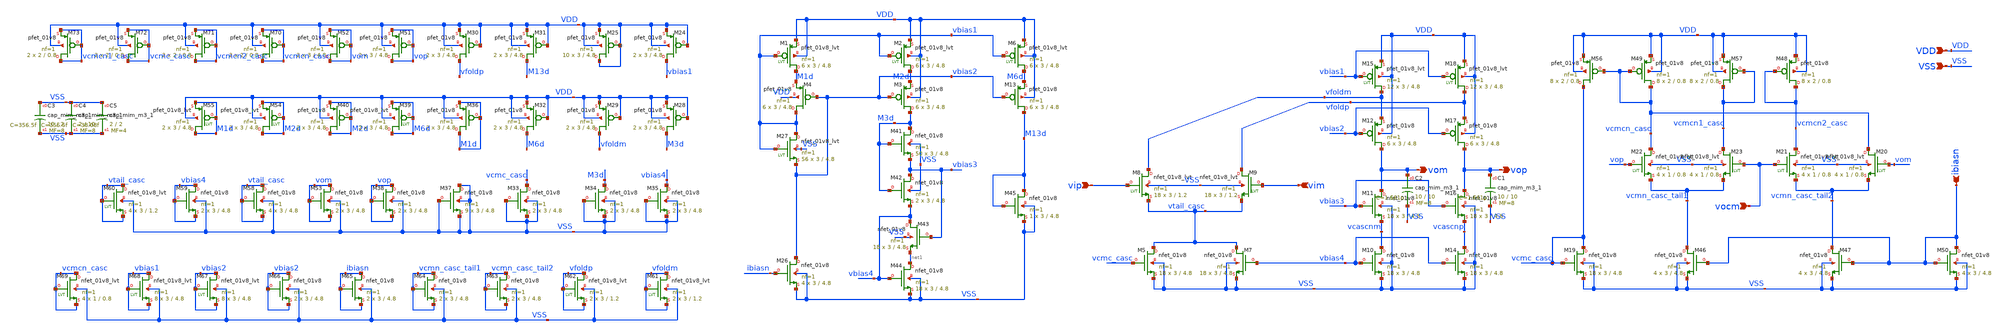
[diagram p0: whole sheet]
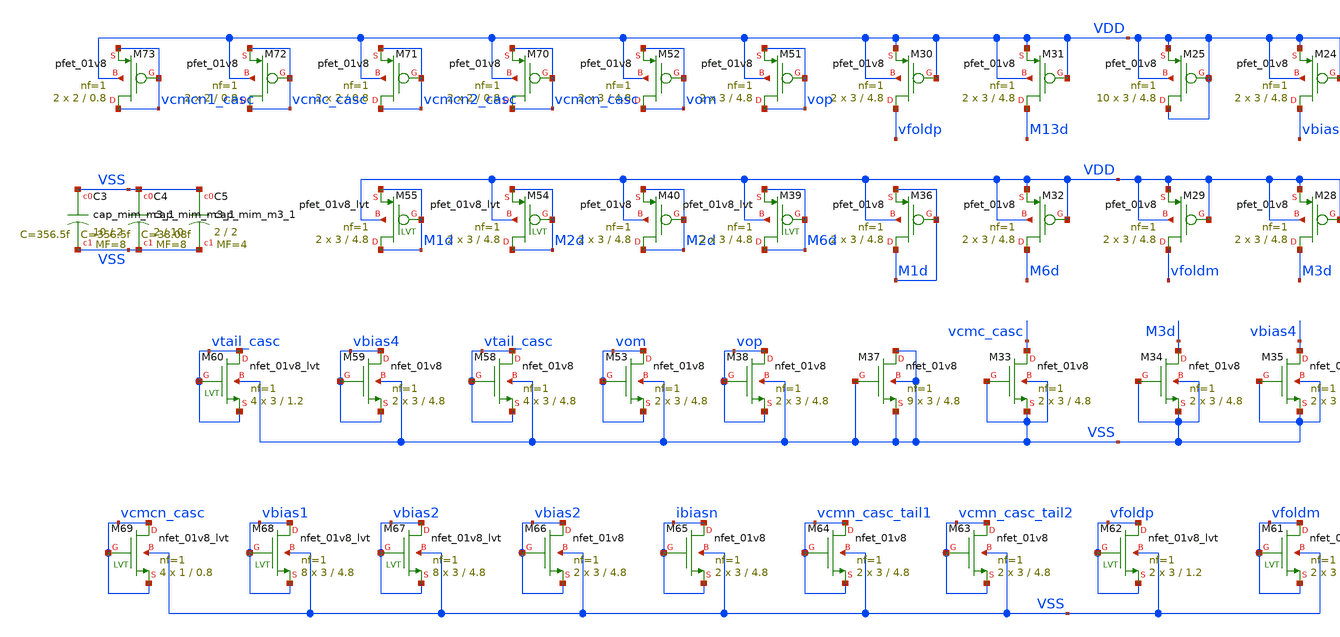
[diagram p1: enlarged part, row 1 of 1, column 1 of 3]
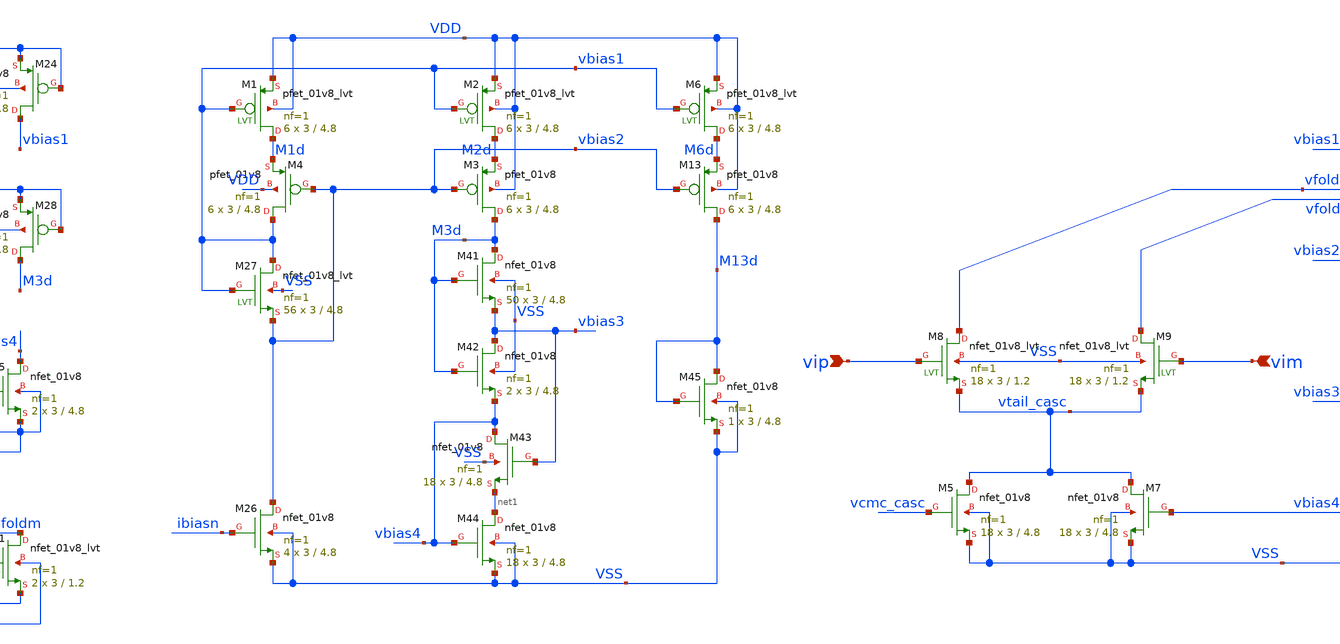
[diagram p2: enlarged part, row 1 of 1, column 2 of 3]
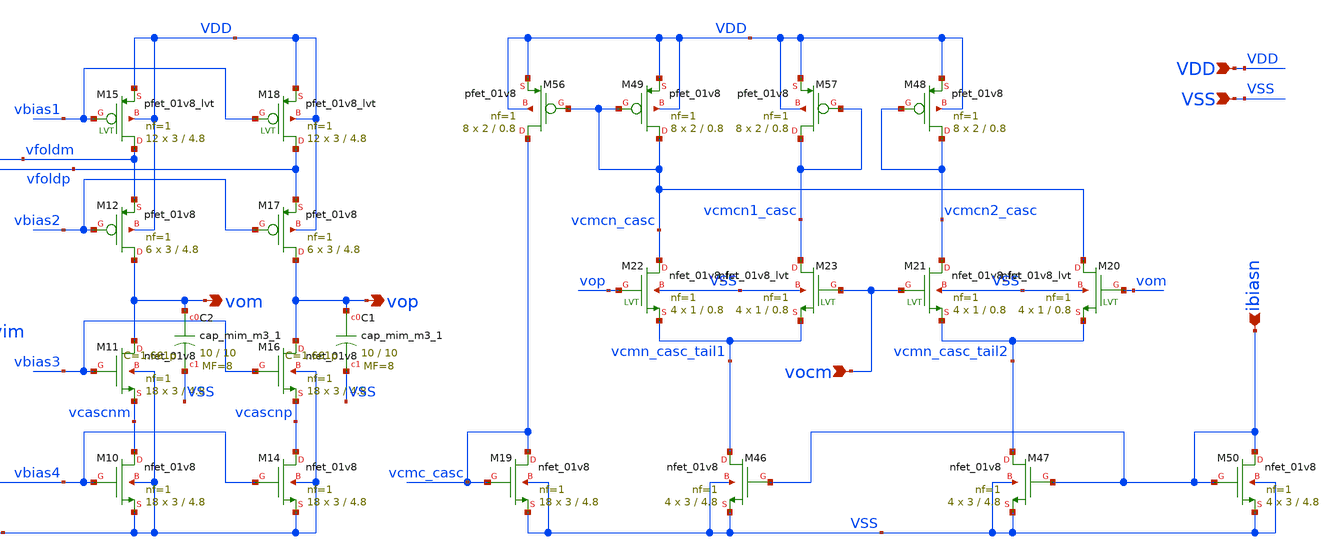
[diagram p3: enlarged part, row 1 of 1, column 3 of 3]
** sch_path: designs/diff_fold_casc_ota_lvs.sch
* Copyright 2020 Stefan Frederik Schippers
* Licensed under the Apache License, Version 2.0 (the "License");
* you may not use this file except in compliance with the License.
* You may obtain a copy of the License at
* https://www.apache.org/licenses/LICENSE-2.0
* Unless required by applicable law or agreed to in writing, software
* distributed under the License is distributed on an "AS IS" BASIS,
* WITHOUT WARRANTIES OR CONDITIONS OF ANY KIND, either express or implied.
* See the License for the specific language governing permissions and
* limitations under the License.
**.subckt diff_fold_casc_ota_lvs vop vom vip vim vocm ibiasn VDD VSS
*.opin vop
*.opin vom
*.ipin vip
*.ipin vim
*.ipin vocm
*.ipin ibiasn
*.ipin VDD
*.ipin VSS
XM41 M3d M3d vbias3 VSS sky130_fd_pr__nfet_01v8 L=4.8 W=3 nf=1 ad='int((nf+1)/2) * W/nf * 0.29' as='int((nf+2)/2) * W/nf * 0.29'
+ pd='2*int((nf+1)/2) * (W/nf + 0.29)' ps='2*int((nf+2)/2) * (W/nf + 0.29)' nrd='0.29 / W' nrs='0.29 / W'
+ sa=0 sb=0 sd=0 mult=50 m=50
XM42 vbias3 M3d vbias4 VSS sky130_fd_pr__nfet_01v8 L=4.8 W=3 nf=1 ad='int((nf+1)/2) * W/nf * 0.29' as='int((nf+2)/2) * W/nf * 0.29'
+ pd='2*int((nf+1)/2) * (W/nf + 0.29)' ps='2*int((nf+2)/2) * (W/nf + 0.29)' nrd='0.29 / W' nrs='0.29 / W'
+ sa=0 sb=0 sd=0 mult=2 m=2
XM43 vbias4 vbias3 net1 VSS sky130_fd_pr__nfet_01v8 L=4.8 W=3 nf=1 ad='int((nf+1)/2) * W/nf * 0.29' as='int((nf+2)/2) * W/nf * 0.29'
+ pd='2*int((nf+1)/2) * (W/nf + 0.29)' ps='2*int((nf+2)/2) * (W/nf + 0.29)' nrd='0.29 / W' nrs='0.29 / W'
+ sa=0 sb=0 sd=0 mult=18 m=18
XM44 net1 vbias4 VSS VSS sky130_fd_pr__nfet_01v8 L=4.8 W=3 nf=1 ad='int((nf+1)/2) * W/nf * 0.29' as='int((nf+2)/2) * W/nf * 0.29'
+ pd='2*int((nf+1)/2) * (W/nf + 0.29)' ps='2*int((nf+2)/2) * (W/nf + 0.29)' nrd='0.29 / W' nrs='0.29 / W'
+ sa=0 sb=0 sd=0 mult=18 m=18
XM45 M13d M13d VSS VSS sky130_fd_pr__nfet_01v8 L=4.8 W=3 nf=1 ad='int((nf+1)/2) * W/nf * 0.29' as='int((nf+2)/2) * W/nf * 0.29'
+ pd='2*int((nf+1)/2) * (W/nf + 0.29)' ps='2*int((nf+2)/2) * (W/nf + 0.29)' nrd='0.29 / W' nrs='0.29 / W'
+ sa=0 sb=0 sd=0 mult=1 m=1
XM46 vcmn_casc_tail1 ibiasn VSS VSS sky130_fd_pr__nfet_01v8 L=4.8 W=3 nf=1 ad='int((nf+1)/2) * W/nf * 0.29'
+ as='int((nf+2)/2) * W/nf * 0.29' pd='2*int((nf+1)/2) * (W/nf + 0.29)' ps='2*int((nf+2)/2) * (W/nf + 0.29)'
+ nrd='0.29 / W' nrs='0.29 / W' sa=0 sb=0 sd=0 mult=4 m=4
XM47 vcmn_casc_tail2 ibiasn VSS VSS sky130_fd_pr__nfet_01v8 L=4.8 W=3 nf=1 ad='int((nf+1)/2) * W/nf * 0.29'
+ as='int((nf+2)/2) * W/nf * 0.29' pd='2*int((nf+1)/2) * (W/nf + 0.29)' ps='2*int((nf+2)/2) * (W/nf + 0.29)'
+ nrd='0.29 / W' nrs='0.29 / W' sa=0 sb=0 sd=0 mult=4 m=4
XM48 vcmcn2_casc vcmcn2_casc VDD VDD sky130_fd_pr__pfet_01v8 L=0.8 W=2 nf=1 ad='int((nf+1)/2) * W/nf * 0.29'
+ as='int((nf+2)/2) * W/nf * 0.29' pd='2*int((nf+1)/2) * (W/nf + 0.29)' ps='2*int((nf+2)/2) * (W/nf + 0.29)'
+ nrd='0.29 / W' nrs='0.29 / W' sa=0 sb=0 sd=0 mult=8 m=8
XM49 vcmcn_casc vcmcn_casc VDD VDD sky130_fd_pr__pfet_01v8 L=0.8 W=2 nf=1 ad='int((nf+1)/2) * W/nf * 0.29'
+ as='int((nf+2)/2) * W/nf * 0.29' pd='2*int((nf+1)/2) * (W/nf + 0.29)' ps='2*int((nf+2)/2) * (W/nf + 0.29)'
+ nrd='0.29 / W' nrs='0.29 / W' sa=0 sb=0 sd=0 mult=8 m=8
XM50 ibiasn ibiasn VSS VSS sky130_fd_pr__nfet_01v8 L=4.8 W=3 nf=1 ad='int((nf+1)/2) * W/nf * 0.29' as='int((nf+2)/2) * W/nf * 0.29'
+ pd='2*int((nf+1)/2) * (W/nf + 0.29)' ps='2*int((nf+2)/2) * (W/nf + 0.29)' nrd='0.29 / W' nrs='0.29 / W'
+ sa=0 sb=0 sd=0 mult=4 m=4
XM56 vcmc_casc vcmcn_casc VDD VDD sky130_fd_pr__pfet_01v8 L=0.8 W=2 nf=1 ad='int((nf+1)/2) * W/nf * 0.29'
+ as='int((nf+2)/2) * W/nf * 0.29' pd='2*int((nf+1)/2) * (W/nf + 0.29)' ps='2*int((nf+2)/2) * (W/nf + 0.29)'
+ nrd='0.29 / W' nrs='0.29 / W' sa=0 sb=0 sd=0 mult=8 m=8
XM57 vcmcn1_casc vcmcn1_casc VDD VDD sky130_fd_pr__pfet_01v8 L=0.8 W=2 nf=1 ad='int((nf+1)/2) * W/nf * 0.29'
+ as='int((nf+2)/2) * W/nf * 0.29' pd='2*int((nf+1)/2) * (W/nf + 0.29)' ps='2*int((nf+2)/2) * (W/nf + 0.29)'
+ nrd='0.29 / W' nrs='0.29 / W' sa=0 sb=0 sd=0 mult=8 m=8
XM1 M1d vbias1 VDD VDD sky130_fd_pr__pfet_01v8_lvt L=4.8 W=3 nf=1 ad='int((nf+1)/2) * W/nf * 0.29' as='int((nf+2)/2) * W/nf * 0.29'
+ pd='2*int((nf+1)/2) * (W/nf + 0.29)' ps='2*int((nf+2)/2) * (W/nf + 0.29)' nrd='0.29 / W' nrs='0.29 / W'
+ sa=0 sb=0 sd=0 mult=6 m=6
XM5 vtail_casc vcmc_casc VSS VSS sky130_fd_pr__nfet_01v8 L=4.8 W=3 nf=1 ad='int((nf+1)/2) * W/nf * 0.29'
+ as='int((nf+2)/2) * W/nf * 0.29' pd='2*int((nf+1)/2) * (W/nf + 0.29)' ps='2*int((nf+2)/2) * (W/nf + 0.29)'
+ nrd='0.29 / W' nrs='0.29 / W' sa=0 sb=0 sd=0 mult=18 m=18
XM8 vfoldm vip vtail_casc VSS sky130_fd_pr__nfet_01v8_lvt L=1.2 W=3 nf=1 ad='int((nf+1)/2) * W/nf * 0.29'
+ as='int((nf+2)/2) * W/nf * 0.29' pd='2*int((nf+1)/2) * (W/nf + 0.29)' ps='2*int((nf+2)/2) * (W/nf + 0.29)'
+ nrd='0.29 / W' nrs='0.29 / W' sa=0 sb=0 sd=0 mult=18 m=18
XM3 M3d vbias2 M2d VDD sky130_fd_pr__pfet_01v8 L=4.8 W=3 nf=1 ad='int((nf+1)/2) * W/nf * 0.29' as='int((nf+2)/2) * W/nf * 0.29'
+ pd='2*int((nf+1)/2) * (W/nf + 0.29)' ps='2*int((nf+2)/2) * (W/nf + 0.29)' nrd='0.29 / W' nrs='0.29 / W'
+ sa=0 sb=0 sd=0 mult=6 m=6
XM2 M2d vbias1 VDD VDD sky130_fd_pr__pfet_01v8_lvt L=4.8 W=3 nf=1 ad='int((nf+1)/2) * W/nf * 0.29' as='int((nf+2)/2) * W/nf * 0.29'
+ pd='2*int((nf+1)/2) * (W/nf + 0.29)' ps='2*int((nf+2)/2) * (W/nf + 0.29)' nrd='0.29 / W' nrs='0.29 / W'
+ sa=0 sb=0 sd=0 mult=6 m=6
XM6 M6d vbias1 VDD VDD sky130_fd_pr__pfet_01v8_lvt L=4.8 W=3 nf=1 ad='int((nf+1)/2) * W/nf * 0.29' as='int((nf+2)/2) * W/nf * 0.29'
+ pd='2*int((nf+1)/2) * (W/nf + 0.29)' ps='2*int((nf+2)/2) * (W/nf + 0.29)' nrd='0.29 / W' nrs='0.29 / W'
+ sa=0 sb=0 sd=0 mult=6 m=6
XM4 vbias1 vbias2 M1d VDD sky130_fd_pr__pfet_01v8 L=4.8 W=3 nf=1 ad='int((nf+1)/2) * W/nf * 0.29' as='int((nf+2)/2) * W/nf * 0.29'
+ pd='2*int((nf+1)/2) * (W/nf + 0.29)' ps='2*int((nf+2)/2) * (W/nf + 0.29)' nrd='0.29 / W' nrs='0.29 / W'
+ sa=0 sb=0 sd=0 mult=6 m=6
XM13 M13d vbias2 M6d VDD sky130_fd_pr__pfet_01v8 L=4.8 W=3 nf=1 ad='int((nf+1)/2) * W/nf * 0.29' as='int((nf+2)/2) * W/nf * 0.29'
+ pd='2*int((nf+1)/2) * (W/nf + 0.29)' ps='2*int((nf+2)/2) * (W/nf + 0.29)' nrd='0.29 / W' nrs='0.29 / W'
+ sa=0 sb=0 sd=0 mult=6 m=6
XM7 vtail_casc vbias4 VSS VSS sky130_fd_pr__nfet_01v8 L=4.8 W=3 nf=1 ad='int((nf+1)/2) * W/nf * 0.29'
+ as='int((nf+2)/2) * W/nf * 0.29' pd='2*int((nf+1)/2) * (W/nf + 0.29)' ps='2*int((nf+2)/2) * (W/nf + 0.29)'
+ nrd='0.29 / W' nrs='0.29 / W' sa=0 sb=0 sd=0 mult=18 m=18
XM10 vcascnm vbias4 VSS VSS sky130_fd_pr__nfet_01v8 L=4.8 W=3 nf=1 ad='int((nf+1)/2) * W/nf * 0.29' as='int((nf+2)/2) * W/nf * 0.29'
+ pd='2*int((nf+1)/2) * (W/nf + 0.29)' ps='2*int((nf+2)/2) * (W/nf + 0.29)' nrd='0.29 / W' nrs='0.29 / W'
+ sa=0 sb=0 sd=0 mult=18 m=18
XM14 vcascnp vbias4 VSS VSS sky130_fd_pr__nfet_01v8 L=4.8 W=3 nf=1 ad='int((nf+1)/2) * W/nf * 0.29' as='int((nf+2)/2) * W/nf * 0.29'
+ pd='2*int((nf+1)/2) * (W/nf + 0.29)' ps='2*int((nf+2)/2) * (W/nf + 0.29)' nrd='0.29 / W' nrs='0.29 / W'
+ sa=0 sb=0 sd=0 mult=18 m=18
XM11 vom vbias3 vcascnm VSS sky130_fd_pr__nfet_01v8 L=4.8 W=3 nf=1 ad='int((nf+1)/2) * W/nf * 0.29' as='int((nf+2)/2) * W/nf * 0.29'
+ pd='2*int((nf+1)/2) * (W/nf + 0.29)' ps='2*int((nf+2)/2) * (W/nf + 0.29)' nrd='0.29 / W' nrs='0.29 / W'
+ sa=0 sb=0 sd=0 mult=18 m=18
XM16 vop vbias3 vcascnp VSS sky130_fd_pr__nfet_01v8 L=4.8 W=3 nf=1 ad='int((nf+1)/2) * W/nf * 0.29' as='int((nf+2)/2) * W/nf * 0.29'
+ pd='2*int((nf+1)/2) * (W/nf + 0.29)' ps='2*int((nf+2)/2) * (W/nf + 0.29)' nrd='0.29 / W' nrs='0.29 / W'
+ sa=0 sb=0 sd=0 mult=18 m=18
XM12 vom vbias2 vfoldm VDD sky130_fd_pr__pfet_01v8 L=4.8 W=3 nf=1 ad='int((nf+1)/2) * W/nf * 0.29' as='int((nf+2)/2) * W/nf * 0.29'
+ pd='2*int((nf+1)/2) * (W/nf + 0.29)' ps='2*int((nf+2)/2) * (W/nf + 0.29)' nrd='0.29 / W' nrs='0.29 / W'
+ sa=0 sb=0 sd=0 mult=6 m=6
XM17 vop vbias2 vfoldp VDD sky130_fd_pr__pfet_01v8 L=4.8 W=3 nf=1 ad='int((nf+1)/2) * W/nf * 0.29' as='int((nf+2)/2) * W/nf * 0.29'
+ pd='2*int((nf+1)/2) * (W/nf + 0.29)' ps='2*int((nf+2)/2) * (W/nf + 0.29)' nrd='0.29 / W' nrs='0.29 / W'
+ sa=0 sb=0 sd=0 mult=6 m=6
XM15 vfoldm vbias1 VDD VDD sky130_fd_pr__pfet_01v8_lvt L=4.8 W=3 nf=1 ad='int((nf+1)/2) * W/nf * 0.29'
+ as='int((nf+2)/2) * W/nf * 0.29' pd='2*int((nf+1)/2) * (W/nf + 0.29)' ps='2*int((nf+2)/2) * (W/nf + 0.29)'
+ nrd='0.29 / W' nrs='0.29 / W' sa=0 sb=0 sd=0 mult=12 m=12
XM18 vfoldp vbias1 VDD VDD sky130_fd_pr__pfet_01v8_lvt L=4.8 W=3 nf=1 ad='int((nf+1)/2) * W/nf * 0.29'
+ as='int((nf+2)/2) * W/nf * 0.29' pd='2*int((nf+1)/2) * (W/nf + 0.29)' ps='2*int((nf+2)/2) * (W/nf + 0.29)'
+ nrd='0.29 / W' nrs='0.29 / W' sa=0 sb=0 sd=0 mult=12 m=12
XM19 vcmc_casc vcmc_casc VSS VSS sky130_fd_pr__nfet_01v8 L=4.8 W=3 nf=1 ad='int((nf+1)/2) * W/nf * 0.29'
+ as='int((nf+2)/2) * W/nf * 0.29' pd='2*int((nf+1)/2) * (W/nf + 0.29)' ps='2*int((nf+2)/2) * (W/nf + 0.29)'
+ nrd='0.29 / W' nrs='0.29 / W' sa=0 sb=0 sd=0 mult=18 m=18
XM20 vcmcn_casc vom vcmn_casc_tail2 VSS sky130_fd_pr__nfet_01v8_lvt L=0.8 W=1 nf=1 ad='int((nf+1)/2) * W/nf * 0.29'
+ as='int((nf+2)/2) * W/nf * 0.29' pd='2*int((nf+1)/2) * (W/nf + 0.29)' ps='2*int((nf+2)/2) * (W/nf + 0.29)'
+ nrd='0.29 / W' nrs='0.29 / W' sa=0 sb=0 sd=0 mult=4 m=4
XM21 vcmcn2_casc vocm vcmn_casc_tail2 VSS sky130_fd_pr__nfet_01v8_lvt L=0.8 W=1 nf=1 ad='int((nf+1)/2) * W/nf * 0.29'
+ as='int((nf+2)/2) * W/nf * 0.29' pd='2*int((nf+1)/2) * (W/nf + 0.29)' ps='2*int((nf+2)/2) * (W/nf + 0.29)'
+ nrd='0.29 / W' nrs='0.29 / W' sa=0 sb=0 sd=0 mult=4 m=4
XM22 vcmcn_casc vop vcmn_casc_tail1 VSS sky130_fd_pr__nfet_01v8_lvt L=0.8 W=1 nf=1 ad='int((nf+1)/2) * W/nf * 0.29'
+ as='int((nf+2)/2) * W/nf * 0.29' pd='2*int((nf+1)/2) * (W/nf + 0.29)' ps='2*int((nf+2)/2) * (W/nf + 0.29)'
+ nrd='0.29 / W' nrs='0.29 / W' sa=0 sb=0 sd=0 mult=4 m=4
XM23 vcmcn1_casc vocm vcmn_casc_tail1 VSS sky130_fd_pr__nfet_01v8_lvt L=0.8 W=1 nf=1 ad='int((nf+1)/2) * W/nf * 0.29'
+ as='int((nf+2)/2) * W/nf * 0.29' pd='2*int((nf+1)/2) * (W/nf + 0.29)' ps='2*int((nf+2)/2) * (W/nf + 0.29)'
+ nrd='0.29 / W' nrs='0.29 / W' sa=0 sb=0 sd=0 mult=4 m=4
XM9 vfoldp vim vtail_casc VSS sky130_fd_pr__nfet_01v8_lvt L=1.2 W=3 nf=1 ad='int((nf+1)/2) * W/nf * 0.29'
+ as='int((nf+2)/2) * W/nf * 0.29' pd='2*int((nf+1)/2) * (W/nf + 0.29)' ps='2*int((nf+2)/2) * (W/nf + 0.29)'
+ nrd='0.29 / W' nrs='0.29 / W' sa=0 sb=0 sd=0 mult=18 m=18
XM26 vbias2 ibiasn VSS VSS sky130_fd_pr__nfet_01v8 L=4.8 W=3 nf=1 ad='int((nf+1)/2) * W/nf * 0.29' as='int((nf+2)/2) * W/nf * 0.29'
+ pd='2*int((nf+1)/2) * (W/nf + 0.29)' ps='2*int((nf+2)/2) * (W/nf + 0.29)' nrd='0.29 / W' nrs='0.29 / W'
+ sa=0 sb=0 sd=0 mult=4 m=4
XM27 vbias1 vbias1 vbias2 VSS sky130_fd_pr__nfet_01v8_lvt L=4.8 W=3 nf=1 ad='int((nf+1)/2) * W/nf * 0.29'
+ as='int((nf+2)/2) * W/nf * 0.29' pd='2*int((nf+1)/2) * (W/nf + 0.29)' ps='2*int((nf+2)/2) * (W/nf + 0.29)'
+ nrd='0.29 / W' nrs='0.29 / W' sa=0 sb=0 sd=0 mult=56 m=56
XM24 vbias1 VDD VDD VDD sky130_fd_pr__pfet_01v8 L=4.8 W=3 nf=1 ad='int((nf+1)/2) * W/nf * 0.29' as='int((nf+2)/2) * W/nf * 0.29'
+ pd='2*int((nf+1)/2) * (W/nf + 0.29)' ps='2*int((nf+2)/2) * (W/nf + 0.29)' nrd='0.29 / W' nrs='0.29 / W'
+ sa=0 sb=0 sd=0 mult=2 m=2
XM25 VDD VDD VDD VDD sky130_fd_pr__pfet_01v8 L=4.8 W=3 nf=1 ad='int((nf+1)/2) * W/nf * 0.29' as='int((nf+2)/2) * W/nf * 0.29'
+ pd='2*int((nf+1)/2) * (W/nf + 0.29)' ps='2*int((nf+2)/2) * (W/nf + 0.29)' nrd='0.29 / W' nrs='0.29 / W'
+ sa=0 sb=0 sd=0 mult=10 m=10
XM28 M3d VDD VDD VDD sky130_fd_pr__pfet_01v8 L=4.8 W=3 nf=1 ad='int((nf+1)/2) * W/nf * 0.29' as='int((nf+2)/2) * W/nf * 0.29'
+ pd='2*int((nf+1)/2) * (W/nf + 0.29)' ps='2*int((nf+2)/2) * (W/nf + 0.29)' nrd='0.29 / W' nrs='0.29 / W'
+ sa=0 sb=0 sd=0 mult=2 m=2
XM29 vfoldm VDD VDD VDD sky130_fd_pr__pfet_01v8 L=4.8 W=3 nf=1 ad='int((nf+1)/2) * W/nf * 0.29' as='int((nf+2)/2) * W/nf * 0.29'
+ pd='2*int((nf+1)/2) * (W/nf + 0.29)' ps='2*int((nf+2)/2) * (W/nf + 0.29)' nrd='0.29 / W' nrs='0.29 / W'
+ sa=0 sb=0 sd=0 mult=2 m=2
XM30 vfoldp VDD VDD VDD sky130_fd_pr__pfet_01v8 L=4.8 W=3 nf=1 ad='int((nf+1)/2) * W/nf * 0.29' as='int((nf+2)/2) * W/nf * 0.29'
+ pd='2*int((nf+1)/2) * (W/nf + 0.29)' ps='2*int((nf+2)/2) * (W/nf + 0.29)' nrd='0.29 / W' nrs='0.29 / W'
+ sa=0 sb=0 sd=0 mult=2 m=2
XM31 M13d VDD VDD VDD sky130_fd_pr__pfet_01v8 L=4.8 W=3 nf=1 ad='int((nf+1)/2) * W/nf * 0.29' as='int((nf+2)/2) * W/nf * 0.29'
+ pd='2*int((nf+1)/2) * (W/nf + 0.29)' ps='2*int((nf+2)/2) * (W/nf + 0.29)' nrd='0.29 / W' nrs='0.29 / W'
+ sa=0 sb=0 sd=0 mult=2 m=2
XM32 M6d VDD VDD VDD sky130_fd_pr__pfet_01v8 L=4.8 W=3 nf=1 ad='int((nf+1)/2) * W/nf * 0.29' as='int((nf+2)/2) * W/nf * 0.29'
+ pd='2*int((nf+1)/2) * (W/nf + 0.29)' ps='2*int((nf+2)/2) * (W/nf + 0.29)' nrd='0.29 / W' nrs='0.29 / W'
+ sa=0 sb=0 sd=0 mult=2 m=2
XM33 vcmc_casc VSS VSS VSS sky130_fd_pr__nfet_01v8 L=4.8 W=3 nf=1 ad='int((nf+1)/2) * W/nf * 0.29' as='int((nf+2)/2) * W/nf * 0.29'
+ pd='2*int((nf+1)/2) * (W/nf + 0.29)' ps='2*int((nf+2)/2) * (W/nf + 0.29)' nrd='0.29 / W' nrs='0.29 / W'
+ sa=0 sb=0 sd=0 mult=2 m=2
XM34 M3d VSS VSS VSS sky130_fd_pr__nfet_01v8 L=4.8 W=3 nf=1 ad='int((nf+1)/2) * W/nf * 0.29' as='int((nf+2)/2) * W/nf * 0.29'
+ pd='2*int((nf+1)/2) * (W/nf + 0.29)' ps='2*int((nf+2)/2) * (W/nf + 0.29)' nrd='0.29 / W' nrs='0.29 / W'
+ sa=0 sb=0 sd=0 mult=2 m=2
XM35 vbias4 VSS VSS VSS sky130_fd_pr__nfet_01v8 L=4.8 W=3 nf=1 ad='int((nf+1)/2) * W/nf * 0.29' as='int((nf+2)/2) * W/nf * 0.29'
+ pd='2*int((nf+1)/2) * (W/nf + 0.29)' ps='2*int((nf+2)/2) * (W/nf + 0.29)' nrd='0.29 / W' nrs='0.29 / W'
+ sa=0 sb=0 sd=0 mult=2 m=2
XM36 M1d M1d M1d VDD sky130_fd_pr__pfet_01v8 L=4.8 W=3 nf=1 ad='int((nf+1)/2) * W/nf * 0.29' as='int((nf+2)/2) * W/nf * 0.29'
+ pd='2*int((nf+1)/2) * (W/nf + 0.29)' ps='2*int((nf+2)/2) * (W/nf + 0.29)' nrd='0.29 / W' nrs='0.29 / W'
+ sa=0 sb=0 sd=0 mult=2 m=2
XM37 VSS VSS VSS VSS sky130_fd_pr__nfet_01v8 L=4.8 W=3 nf=1 ad='int((nf+1)/2) * W/nf * 0.29' as='int((nf+2)/2) * W/nf * 0.29'
+ pd='2*int((nf+1)/2) * (W/nf + 0.29)' ps='2*int((nf+2)/2) * (W/nf + 0.29)' nrd='0.29 / W' nrs='0.29 / W'
+ sa=0 sb=0 sd=0 mult=9 m=9
XM38 vop vop vop VSS sky130_fd_pr__nfet_01v8 L=4.8 W=3 nf=1 ad='int((nf+1)/2) * W/nf * 0.29' as='int((nf+2)/2) * W/nf * 0.29'
+ pd='2*int((nf+1)/2) * (W/nf + 0.29)' ps='2*int((nf+2)/2) * (W/nf + 0.29)' nrd='0.29 / W' nrs='0.29 / W'
+ sa=0 sb=0 sd=0 mult=2 m=2
XM40 M2d M2d M2d VDD sky130_fd_pr__pfet_01v8 L=4.8 W=3 nf=1 ad='int((nf+1)/2) * W/nf * 0.29' as='int((nf+2)/2) * W/nf * 0.29'
+ pd='2*int((nf+1)/2) * (W/nf + 0.29)' ps='2*int((nf+2)/2) * (W/nf + 0.29)' nrd='0.29 / W' nrs='0.29 / W'
+ sa=0 sb=0 sd=0 mult=2 m=2
XM51 vop vop vop VDD sky130_fd_pr__pfet_01v8 L=4.8 W=3 nf=1 ad='int((nf+1)/2) * W/nf * 0.29' as='int((nf+2)/2) * W/nf * 0.29'
+ pd='2*int((nf+1)/2) * (W/nf + 0.29)' ps='2*int((nf+2)/2) * (W/nf + 0.29)' nrd='0.29 / W' nrs='0.29 / W'
+ sa=0 sb=0 sd=0 mult=2 m=2
XM52 vom vom vom VDD sky130_fd_pr__pfet_01v8 L=4.8 W=3 nf=1 ad='int((nf+1)/2) * W/nf * 0.29' as='int((nf+2)/2) * W/nf * 0.29'
+ pd='2*int((nf+1)/2) * (W/nf + 0.29)' ps='2*int((nf+2)/2) * (W/nf + 0.29)' nrd='0.29 / W' nrs='0.29 / W'
+ sa=0 sb=0 sd=0 mult=2 m=2
XM53 vom vom vom VSS sky130_fd_pr__nfet_01v8 L=4.8 W=3 nf=1 ad='int((nf+1)/2) * W/nf * 0.29' as='int((nf+2)/2) * W/nf * 0.29'
+ pd='2*int((nf+1)/2) * (W/nf + 0.29)' ps='2*int((nf+2)/2) * (W/nf + 0.29)' nrd='0.29 / W' nrs='0.29 / W'
+ sa=0 sb=0 sd=0 mult=2 m=2
XM54 M2d M2d M2d VDD sky130_fd_pr__pfet_01v8_lvt L=4.8 W=3 nf=1 ad='int((nf+1)/2) * W/nf * 0.29' as='int((nf+2)/2) * W/nf * 0.29'
+ pd='2*int((nf+1)/2) * (W/nf + 0.29)' ps='2*int((nf+2)/2) * (W/nf + 0.29)' nrd='0.29 / W' nrs='0.29 / W'
+ sa=0 sb=0 sd=0 mult=2 m=2
XM55 M1d M1d M1d VDD sky130_fd_pr__pfet_01v8_lvt L=4.8 W=3 nf=1 ad='int((nf+1)/2) * W/nf * 0.29' as='int((nf+2)/2) * W/nf * 0.29'
+ pd='2*int((nf+1)/2) * (W/nf + 0.29)' ps='2*int((nf+2)/2) * (W/nf + 0.29)' nrd='0.29 / W' nrs='0.29 / W'
+ sa=0 sb=0 sd=0 mult=2 m=2
XM39 M6d M6d M6d VDD sky130_fd_pr__pfet_01v8_lvt L=4.8 W=3 nf=1 ad='int((nf+1)/2) * W/nf * 0.29' as='int((nf+2)/2) * W/nf * 0.29'
+ pd='2*int((nf+1)/2) * (W/nf + 0.29)' ps='2*int((nf+2)/2) * (W/nf + 0.29)' nrd='0.29 / W' nrs='0.29 / W'
+ sa=0 sb=0 sd=0 mult=2 m=2
XM58 vtail_casc vtail_casc vtail_casc VSS sky130_fd_pr__nfet_01v8 L=4.8 W=3 nf=1 ad='int((nf+1)/2) * W/nf * 0.29'
+ as='int((nf+2)/2) * W/nf * 0.29' pd='2*int((nf+1)/2) * (W/nf + 0.29)' ps='2*int((nf+2)/2) * (W/nf + 0.29)'
+ nrd='0.29 / W' nrs='0.29 / W' sa=0 sb=0 sd=0 mult=4 m=4
XM59 vbias4 vbias4 vbias4 VSS sky130_fd_pr__nfet_01v8 L=4.8 W=3 nf=1 ad='int((nf+1)/2) * W/nf * 0.29'
+ as='int((nf+2)/2) * W/nf * 0.29' pd='2*int((nf+1)/2) * (W/nf + 0.29)' ps='2*int((nf+2)/2) * (W/nf + 0.29)'
+ nrd='0.29 / W' nrs='0.29 / W' sa=0 sb=0 sd=0 mult=2 m=2
XM60 vtail_casc vtail_casc vtail_casc VSS sky130_fd_pr__nfet_01v8_lvt L=1.2 W=3 nf=1 ad='int((nf+1)/2) * W/nf * 0.29'
+ as='int((nf+2)/2) * W/nf * 0.29' pd='2*int((nf+1)/2) * (W/nf + 0.29)' ps='2*int((nf+2)/2) * (W/nf + 0.29)'
+ nrd='0.29 / W' nrs='0.29 / W' sa=0 sb=0 sd=0 mult=4 m=4
XM61 vfoldm vfoldm vfoldm VSS sky130_fd_pr__nfet_01v8_lvt L=1.2 W=3 nf=1 ad='int((nf+1)/2) * W/nf * 0.29'
+ as='int((nf+2)/2) * W/nf * 0.29' pd='2*int((nf+1)/2) * (W/nf + 0.29)' ps='2*int((nf+2)/2) * (W/nf + 0.29)'
+ nrd='0.29 / W' nrs='0.29 / W' sa=0 sb=0 sd=0 mult=2 m=2
XM62 vfoldp vfoldp vfoldp VSS sky130_fd_pr__nfet_01v8_lvt L=1.2 W=3 nf=1 ad='int((nf+1)/2) * W/nf * 0.29'
+ as='int((nf+2)/2) * W/nf * 0.29' pd='2*int((nf+1)/2) * (W/nf + 0.29)' ps='2*int((nf+2)/2) * (W/nf + 0.29)'
+ nrd='0.29 / W' nrs='0.29 / W' sa=0 sb=0 sd=0 mult=2 m=2
XM63 vcmn_casc_tail2 vcmn_casc_tail2 vcmn_casc_tail2 VSS sky130_fd_pr__nfet_01v8 L=4.8 W=3 nf=1 ad='int((nf+1)/2) * W/nf * 0.29'
+ as='int((nf+2)/2) * W/nf * 0.29' pd='2*int((nf+1)/2) * (W/nf + 0.29)' ps='2*int((nf+2)/2) * (W/nf + 0.29)'
+ nrd='0.29 / W' nrs='0.29 / W' sa=0 sb=0 sd=0 mult=2 m=2
XM64 vcmn_casc_tail1 vcmn_casc_tail1 vcmn_casc_tail1 VSS sky130_fd_pr__nfet_01v8 L=4.8 W=3 nf=1 ad='int((nf+1)/2) * W/nf * 0.29'
+ as='int((nf+2)/2) * W/nf * 0.29' pd='2*int((nf+1)/2) * (W/nf + 0.29)' ps='2*int((nf+2)/2) * (W/nf + 0.29)'
+ nrd='0.29 / W' nrs='0.29 / W' sa=0 sb=0 sd=0 mult=2 m=2
XM65 ibiasn ibiasn ibiasn VSS sky130_fd_pr__nfet_01v8 L=4.8 W=3 nf=1 ad='int((nf+1)/2) * W/nf * 0.29'
+ as='int((nf+2)/2) * W/nf * 0.29' pd='2*int((nf+1)/2) * (W/nf + 0.29)' ps='2*int((nf+2)/2) * (W/nf + 0.29)'
+ nrd='0.29 / W' nrs='0.29 / W' sa=0 sb=0 sd=0 mult=2 m=2
XM66 vbias2 vbias2 vbias2 VSS sky130_fd_pr__nfet_01v8 L=4.8 W=3 nf=1 ad='int((nf+1)/2) * W/nf * 0.29'
+ as='int((nf+2)/2) * W/nf * 0.29' pd='2*int((nf+1)/2) * (W/nf + 0.29)' ps='2*int((nf+2)/2) * (W/nf + 0.29)'
+ nrd='0.29 / W' nrs='0.29 / W' sa=0 sb=0 sd=0 mult=2 m=2
XM67 vbias2 vbias2 vbias2 VSS sky130_fd_pr__nfet_01v8_lvt L=4.8 W=3 nf=1 ad='int((nf+1)/2) * W/nf * 0.29'
+ as='int((nf+2)/2) * W/nf * 0.29' pd='2*int((nf+1)/2) * (W/nf + 0.29)' ps='2*int((nf+2)/2) * (W/nf + 0.29)'
+ nrd='0.29 / W' nrs='0.29 / W' sa=0 sb=0 sd=0 mult=8 m=8
XM68 vbias1 vbias1 vbias1 VSS sky130_fd_pr__nfet_01v8_lvt L=4.8 W=3 nf=1 ad='int((nf+1)/2) * W/nf * 0.29'
+ as='int((nf+2)/2) * W/nf * 0.29' pd='2*int((nf+1)/2) * (W/nf + 0.29)' ps='2*int((nf+2)/2) * (W/nf + 0.29)'
+ nrd='0.29 / W' nrs='0.29 / W' sa=0 sb=0 sd=0 mult=8 m=8
XM69 vcmcn_casc vcmcn_casc vcmcn_casc VSS sky130_fd_pr__nfet_01v8_lvt L=0.8 W=1 nf=1 ad='int((nf+1)/2) * W/nf * 0.29'
+ as='int((nf+2)/2) * W/nf * 0.29' pd='2*int((nf+1)/2) * (W/nf + 0.29)' ps='2*int((nf+2)/2) * (W/nf + 0.29)'
+ nrd='0.29 / W' nrs='0.29 / W' sa=0 sb=0 sd=0 mult=4 m=4
XM70 vcmcn_casc vcmcn_casc vcmcn_casc VDD sky130_fd_pr__pfet_01v8 L=0.8 W=2 nf=1 ad='int((nf+1)/2) * W/nf * 0.29'
+ as='int((nf+2)/2) * W/nf * 0.29' pd='2*int((nf+1)/2) * (W/nf + 0.29)' ps='2*int((nf+2)/2) * (W/nf + 0.29)'
+ nrd='0.29 / W' nrs='0.29 / W' sa=0 sb=0 sd=0 mult=2 m=2
XM71 vcmcn2_casc vcmcn2_casc vcmcn2_casc VDD sky130_fd_pr__pfet_01v8 L=0.8 W=2 nf=1 ad='int((nf+1)/2) * W/nf * 0.29'
+ as='int((nf+2)/2) * W/nf * 0.29' pd='2*int((nf+1)/2) * (W/nf + 0.29)' ps='2*int((nf+2)/2) * (W/nf + 0.29)'
+ nrd='0.29 / W' nrs='0.29 / W' sa=0 sb=0 sd=0 mult=2 m=2
XM72 vcmc_casc vcmc_casc vcmc_casc VDD sky130_fd_pr__pfet_01v8 L=0.8 W=2 nf=1 ad='int((nf+1)/2) * W/nf * 0.29'
+ as='int((nf+2)/2) * W/nf * 0.29' pd='2*int((nf+1)/2) * (W/nf + 0.29)' ps='2*int((nf+2)/2) * (W/nf + 0.29)'
+ nrd='0.29 / W' nrs='0.29 / W' sa=0 sb=0 sd=0 mult=2 m=2
XM73 vcmcn1_casc vcmcn1_casc vcmcn1_casc VDD sky130_fd_pr__pfet_01v8 L=0.8 W=2 nf=1 ad='int((nf+1)/2) * W/nf * 0.29'
+ as='int((nf+2)/2) * W/nf * 0.29' pd='2*int((nf+1)/2) * (W/nf + 0.29)' ps='2*int((nf+2)/2) * (W/nf + 0.29)'
+ nrd='0.29 / W' nrs='0.29 / W' sa=0 sb=0 sd=0 mult=2 m=2
XC1 vop VSS sky130_fd_pr__cap_mim_m3_1 W=10 L=10 MF=8 m=8
XC2 vom VSS sky130_fd_pr__cap_mim_m3_1 W=10 L=10 MF=8 m=8
XC3 VSS VSS sky130_fd_pr__cap_mim_m3_1 W=10 L=2 MF=8 m=8
XC4 VSS VSS sky130_fd_pr__cap_mim_m3_1 W=2 L=10 MF=8 m=8
XC5 VSS VSS sky130_fd_pr__cap_mim_m3_1 W=2 L=2 MF=4 m=4
**.ends
.end
